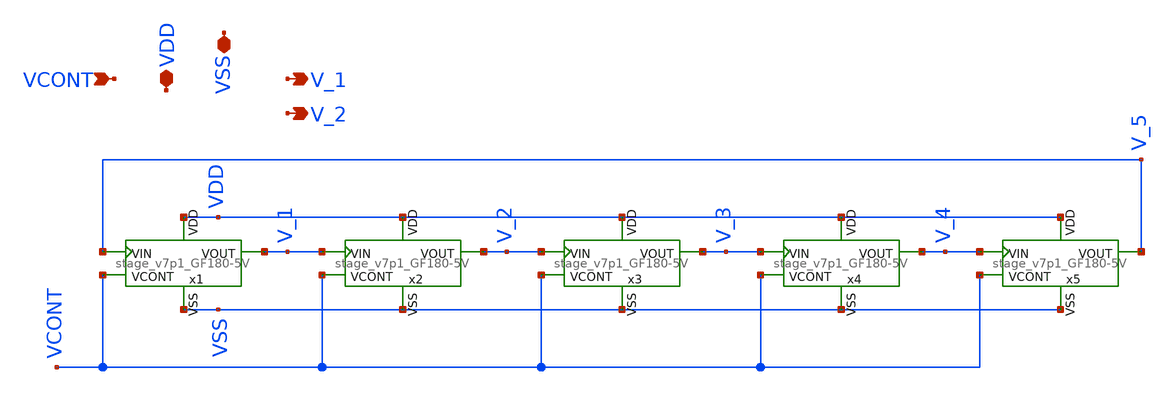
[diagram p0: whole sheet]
** sch_path: xschem/vco/Esm22_CMOSVCOlowG_v7p1_GF180-5V.sch
**.subckt Esm22_CMOSVCOlowG_v7p1_GF180-5V VCONT VDD VSS V_1 V_2
*.ipin VCONT
*.iopin VDD
*.iopin VSS
*.opin V_1
*.opin V_2
x1 VDD VCONT V_1 V_5 VSS stage_v7p1_GF180-5V
x2 VDD VCONT V_2 V_1 VSS stage_v7p1_GF180-5V
x3 VDD VCONT V_3 V_2 VSS stage_v7p1_GF180-5V
x4 VDD VCONT V_4 V_3 VSS stage_v7p1_GF180-5V
x5 VDD VCONT V_5 V_4 VSS stage_v7p1_GF180-5V
**.ends

* expanding   symbol:  vco/stage_v7p1_GF180-5V.sym # of pins=5
** sym_path: xschem/vco/stage_v7p1_GF180-5V.sym
** sch_path: xschem/vco/stage_v7p1_GF180-5V.sch
.subckt stage_v7p1_GF180-5V VDD VCONT VOUT VIN VSS
*.ipin VIN
*.opin VOUT
*.iopin VDD
*.iopin VSS
*.ipin VCONT
XMN1 net4 net4 VSS VSS nfet_05v0 L=0.70u W=7u nf=7 ad='int((nf+1)/2) * W/nf * 0.18u' as='int((nf+2)/2) * W/nf * 0.18u'
+ pd='2*int((nf+1)/2) * (W/nf + 0.18u)' ps='2*int((nf+2)/2) * (W/nf + 0.18u)' nrd='0.18u / W' nrs='0.18u / W'
+ sa=0 sb=0 sd=0 m=1
XMN2 net3 net4 VSS VSS nfet_05v0 L=0.70u W=7u nf=7 ad='int((nf+1)/2) * W/nf * 0.18u' as='int((nf+2)/2) * W/nf * 0.18u'
+ pd='2*int((nf+1)/2) * (W/nf + 0.18u)' ps='2*int((nf+2)/2) * (W/nf + 0.18u)' nrd='0.18u / W' nrs='0.18u / W'
+ sa=0 sb=0 sd=0 m=1
XMN3 net2 net4 VSS VSS nfet_05v0 L=0.70u W=4u nf=4 ad='int((nf+1)/2) * W/nf * 0.18u' as='int((nf+2)/2) * W/nf * 0.18u'
+ pd='2*int((nf+1)/2) * (W/nf + 0.18u)' ps='2*int((nf+2)/2) * (W/nf + 0.18u)' nrd='0.18u / W' nrs='0.18u / W'
+ sa=0 sb=0 sd=0 m=1
XMN4 VOUT VIN net2 VSS nfet_05v0 L=5u W=2u nf=1 ad='int((nf+1)/2) * W/nf * 0.18u' as='int((nf+2)/2) * W/nf * 0.18u'
+ pd='2*int((nf+1)/2) * (W/nf + 0.18u)' ps='2*int((nf+2)/2) * (W/nf + 0.18u)' nrd='0.18u / W' nrs='0.18u / W'
+ sa=0 sb=0 sd=0 m=1
XMP2 net3 net3 VDD VDD pfet_05v0 L=4u W=8u nf=8 ad='int((nf+1)/2) * W/nf * 0.18u' as='int((nf+2)/2) * W/nf * 0.18u'
+ pd='2*int((nf+1)/2) * (W/nf + 0.18u)' ps='2*int((nf+2)/2) * (W/nf + 0.18u)' nrd='0.18u / W' nrs='0.18u / W'
+ sa=0 sb=0 sd=0 m=1
XMP3 net1 net3 VDD VDD pfet_05v0 L=4u W=5u nf=5 ad='int((nf+1)/2) * W/nf * 0.18u' as='int((nf+2)/2) * W/nf * 0.18u'
+ pd='2*int((nf+1)/2) * (W/nf + 0.18u)' ps='2*int((nf+2)/2) * (W/nf + 0.18u)' nrd='0.18u / W' nrs='0.18u / W'
+ sa=0 sb=0 sd=0 m=1
XMP1 net4 VCONT VDD VDD pfet_05v0 L=7u W=0.5u nf=1 ad='int((nf+1)/2) * W/nf * 0.18u' as='int((nf+2)/2) * W/nf * 0.18u'
+ pd='2*int((nf+1)/2) * (W/nf + 0.18u)' ps='2*int((nf+2)/2) * (W/nf + 0.18u)' nrd='0.18u / W' nrs='0.18u / W'
+ sa=0 sb=0 sd=0 m=1
XMP4 VOUT VIN net1 VDD pfet_05v0 L=5u W=5u nf=1 ad='int((nf+1)/2) * W/nf * 0.18u' as='int((nf+2)/2) * W/nf * 0.18u'
+ pd='2*int((nf+1)/2) * (W/nf + 0.18u)' ps='2*int((nf+2)/2) * (W/nf + 0.18u)' nrd='0.18u / W' nrs='0.18u / W'
+ sa=0 sb=0 sd=0 m=1
XMP5 net4 VSS VDD VDD pfet_05v0 L=7u W=0.5u nf=1 ad='int((nf+1)/2) * W/nf * 0.18u' as='int((nf+2)/2) * W/nf * 0.18u'
+ pd='2*int((nf+1)/2) * (W/nf + 0.18u)' ps='2*int((nf+2)/2) * (W/nf + 0.18u)' nrd='0.18u / W' nrs='0.18u / W'
+ sa=0 sb=0 sd=0 m=1
.ends

.end
